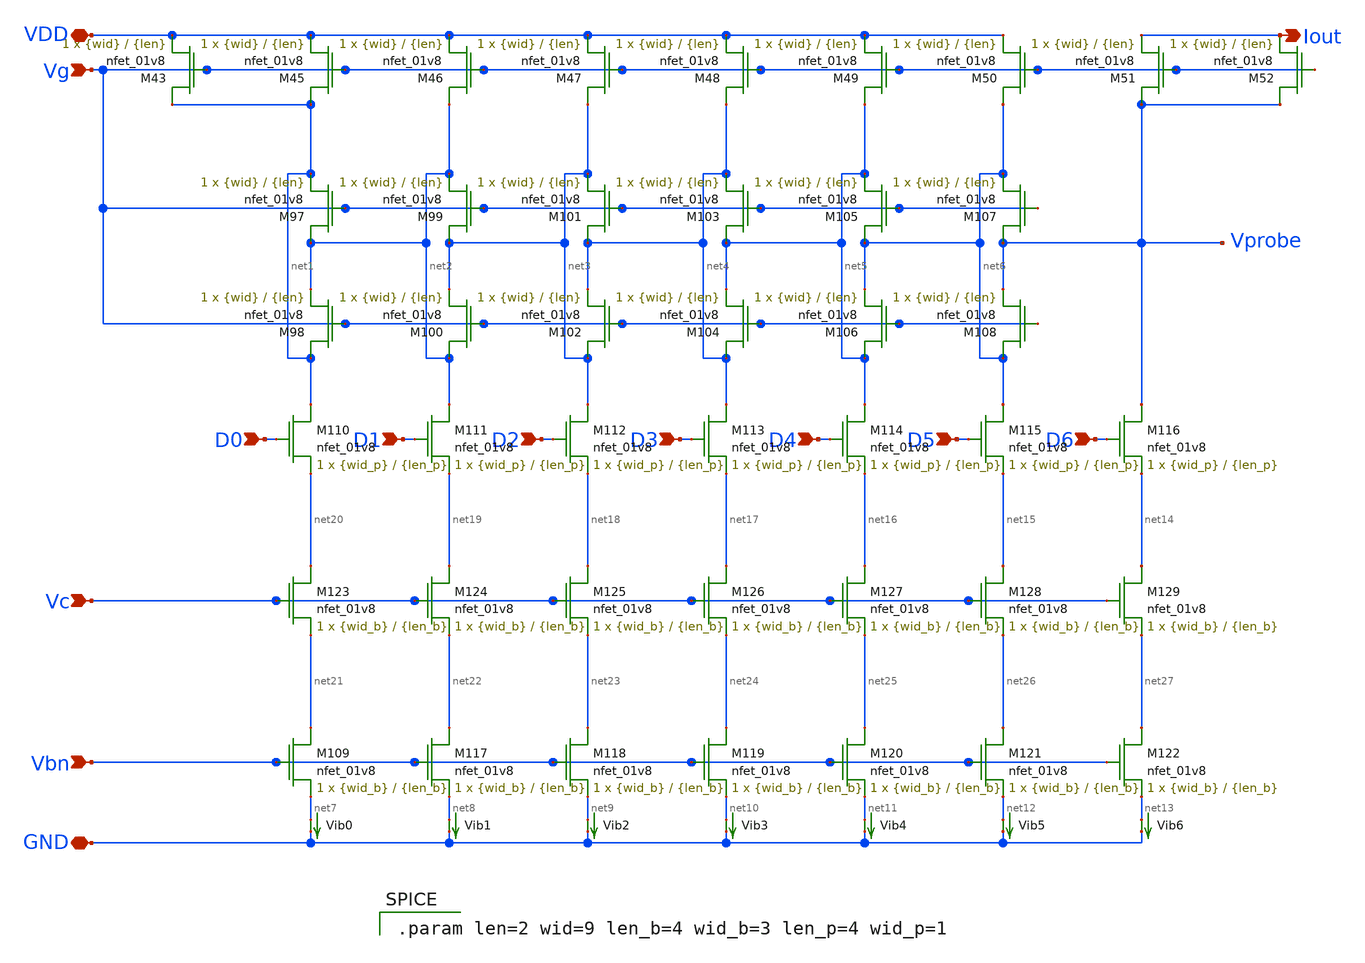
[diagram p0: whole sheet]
** sch_path: mp3/Layout_Schem_Designs/ladder_lds.sch
**.subckt ladder_lds VDD Iout Vg Vbn GND D0 D1 D2 D3 D4 D5 D6 Vc
*.iopin VDD
*.opin Iout
*.ipin Vg
*.ipin Vbn
*.iopin GND
*.ipin D0
*.ipin D1
*.ipin D2
*.ipin D3
*.ipin D4
*.ipin D5
*.ipin D6
*.ipin Vc
XM43 net1 Vg VDD GND sky130_fd_pr__nfet_01v8 L={len} W={wid} nf=1 ad='int((nf+1)/2) * W/nf * 0.29' as='int((nf+2)/2) * W/nf * 0.29'
+ pd='2*int((nf+1)/2) * (W/nf + 0.29)' ps='2*int((nf+2)/2) * (W/nf + 0.29)' nrd='0.29 / W' nrs='0.29 / W'
+ sa=0 sb=0 sd=0 mult=1 m=1
XM45 net1 Vg VDD GND sky130_fd_pr__nfet_01v8 L={len} W={wid} nf=1 ad='int((nf+1)/2) * W/nf * 0.29' as='int((nf+2)/2) * W/nf * 0.29'
+ pd='2*int((nf+1)/2) * (W/nf + 0.29)' ps='2*int((nf+2)/2) * (W/nf + 0.29)' nrd='0.29 / W' nrs='0.29 / W'
+ sa=0 sb=0 sd=0 mult=1 m=1
XM46 net2 Vg VDD GND sky130_fd_pr__nfet_01v8 L={len} W={wid} nf=1 ad='int((nf+1)/2) * W/nf * 0.29' as='int((nf+2)/2) * W/nf * 0.29'
+ pd='2*int((nf+1)/2) * (W/nf + 0.29)' ps='2*int((nf+2)/2) * (W/nf + 0.29)' nrd='0.29 / W' nrs='0.29 / W'
+ sa=0 sb=0 sd=0 mult=1 m=1
XM47 net3 Vg VDD GND sky130_fd_pr__nfet_01v8 L={len} W={wid} nf=1 ad='int((nf+1)/2) * W/nf * 0.29' as='int((nf+2)/2) * W/nf * 0.29'
+ pd='2*int((nf+1)/2) * (W/nf + 0.29)' ps='2*int((nf+2)/2) * (W/nf + 0.29)' nrd='0.29 / W' nrs='0.29 / W'
+ sa=0 sb=0 sd=0 mult=1 m=1
XM48 net4 Vg VDD GND sky130_fd_pr__nfet_01v8 L={len} W={wid} nf=1 ad='int((nf+1)/2) * W/nf * 0.29' as='int((nf+2)/2) * W/nf * 0.29'
+ pd='2*int((nf+1)/2) * (W/nf + 0.29)' ps='2*int((nf+2)/2) * (W/nf + 0.29)' nrd='0.29 / W' nrs='0.29 / W'
+ sa=0 sb=0 sd=0 mult=1 m=1
XM49 net5 Vg VDD GND sky130_fd_pr__nfet_01v8 L={len} W={wid} nf=1 ad='int((nf+1)/2) * W/nf * 0.29' as='int((nf+2)/2) * W/nf * 0.29'
+ pd='2*int((nf+1)/2) * (W/nf + 0.29)' ps='2*int((nf+2)/2) * (W/nf + 0.29)' nrd='0.29 / W' nrs='0.29 / W'
+ sa=0 sb=0 sd=0 mult=1 m=1
XM50 net6 Vg VDD GND sky130_fd_pr__nfet_01v8 L={len} W={wid} nf=1 ad='int((nf+1)/2) * W/nf * 0.29' as='int((nf+2)/2) * W/nf * 0.29'
+ pd='2*int((nf+1)/2) * (W/nf + 0.29)' ps='2*int((nf+2)/2) * (W/nf + 0.29)' nrd='0.29 / W' nrs='0.29 / W'
+ sa=0 sb=0 sd=0 mult=1 m=1
XM51 Vprobe Vg Iout GND sky130_fd_pr__nfet_01v8 L={len} W={wid} nf=1 ad='int((nf+1)/2) * W/nf * 0.29'
+ as='int((nf+2)/2) * W/nf * 0.29' pd='2*int((nf+1)/2) * (W/nf + 0.29)' ps='2*int((nf+2)/2) * (W/nf + 0.29)'
+ nrd='0.29 / W' nrs='0.29 / W' sa=0 sb=0 sd=0 mult=1 m=1
XM52 Vprobe Vg Iout GND sky130_fd_pr__nfet_01v8 L={len} W={wid} nf=1 ad='int((nf+1)/2) * W/nf * 0.29'
+ as='int((nf+2)/2) * W/nf * 0.29' pd='2*int((nf+1)/2) * (W/nf + 0.29)' ps='2*int((nf+2)/2) * (W/nf + 0.29)'
+ nrd='0.29 / W' nrs='0.29 / W' sa=0 sb=0 sd=0 mult=1 m=1
XM97 net2 Vg net1 GND sky130_fd_pr__nfet_01v8 L={len} W={wid} nf=1 ad='int((nf+1)/2) * W/nf * 0.29' as='int((nf+2)/2) * W/nf * 0.29'
+ pd='2*int((nf+1)/2) * (W/nf + 0.29)' ps='2*int((nf+2)/2) * (W/nf + 0.29)' nrd='0.29 / W' nrs='0.29 / W'
+ sa=0 sb=0 sd=0 mult=1 m=1
XM98 net1 Vg net2 GND sky130_fd_pr__nfet_01v8 L={len} W={wid} nf=1 ad='int((nf+1)/2) * W/nf * 0.29' as='int((nf+2)/2) * W/nf * 0.29'
+ pd='2*int((nf+1)/2) * (W/nf + 0.29)' ps='2*int((nf+2)/2) * (W/nf + 0.29)' nrd='0.29 / W' nrs='0.29 / W'
+ sa=0 sb=0 sd=0 mult=1 m=1
XM99 net3 Vg net2 GND sky130_fd_pr__nfet_01v8 L={len} W={wid} nf=1 ad='int((nf+1)/2) * W/nf * 0.29' as='int((nf+2)/2) * W/nf * 0.29'
+ pd='2*int((nf+1)/2) * (W/nf + 0.29)' ps='2*int((nf+2)/2) * (W/nf + 0.29)' nrd='0.29 / W' nrs='0.29 / W'
+ sa=0 sb=0 sd=0 mult=1 m=1
XM100 net2 Vg net3 GND sky130_fd_pr__nfet_01v8 L={len} W={wid} nf=1 ad='int((nf+1)/2) * W/nf * 0.29'
+ as='int((nf+2)/2) * W/nf * 0.29' pd='2*int((nf+1)/2) * (W/nf + 0.29)' ps='2*int((nf+2)/2) * (W/nf + 0.29)'
+ nrd='0.29 / W' nrs='0.29 / W' sa=0 sb=0 sd=0 mult=1 m=1
XM101 net4 Vg net3 GND sky130_fd_pr__nfet_01v8 L={len} W={wid} nf=1 ad='int((nf+1)/2) * W/nf * 0.29'
+ as='int((nf+2)/2) * W/nf * 0.29' pd='2*int((nf+1)/2) * (W/nf + 0.29)' ps='2*int((nf+2)/2) * (W/nf + 0.29)'
+ nrd='0.29 / W' nrs='0.29 / W' sa=0 sb=0 sd=0 mult=1 m=1
XM102 net3 Vg net4 GND sky130_fd_pr__nfet_01v8 L={len} W={wid} nf=1 ad='int((nf+1)/2) * W/nf * 0.29'
+ as='int((nf+2)/2) * W/nf * 0.29' pd='2*int((nf+1)/2) * (W/nf + 0.29)' ps='2*int((nf+2)/2) * (W/nf + 0.29)'
+ nrd='0.29 / W' nrs='0.29 / W' sa=0 sb=0 sd=0 mult=1 m=1
XM103 net5 Vg net4 GND sky130_fd_pr__nfet_01v8 L={len} W={wid} nf=1 ad='int((nf+1)/2) * W/nf * 0.29'
+ as='int((nf+2)/2) * W/nf * 0.29' pd='2*int((nf+1)/2) * (W/nf + 0.29)' ps='2*int((nf+2)/2) * (W/nf + 0.29)'
+ nrd='0.29 / W' nrs='0.29 / W' sa=0 sb=0 sd=0 mult=1 m=1
XM104 net4 Vg net5 GND sky130_fd_pr__nfet_01v8 L={len} W={wid} nf=1 ad='int((nf+1)/2) * W/nf * 0.29'
+ as='int((nf+2)/2) * W/nf * 0.29' pd='2*int((nf+1)/2) * (W/nf + 0.29)' ps='2*int((nf+2)/2) * (W/nf + 0.29)'
+ nrd='0.29 / W' nrs='0.29 / W' sa=0 sb=0 sd=0 mult=1 m=1
XM105 net6 Vg net5 GND sky130_fd_pr__nfet_01v8 L={len} W={wid} nf=1 ad='int((nf+1)/2) * W/nf * 0.29'
+ as='int((nf+2)/2) * W/nf * 0.29' pd='2*int((nf+1)/2) * (W/nf + 0.29)' ps='2*int((nf+2)/2) * (W/nf + 0.29)'
+ nrd='0.29 / W' nrs='0.29 / W' sa=0 sb=0 sd=0 mult=1 m=1
XM106 net5 Vg net6 GND sky130_fd_pr__nfet_01v8 L={len} W={wid} nf=1 ad='int((nf+1)/2) * W/nf * 0.29'
+ as='int((nf+2)/2) * W/nf * 0.29' pd='2*int((nf+1)/2) * (W/nf + 0.29)' ps='2*int((nf+2)/2) * (W/nf + 0.29)'
+ nrd='0.29 / W' nrs='0.29 / W' sa=0 sb=0 sd=0 mult=1 m=1
XM107 Vprobe Vg net6 GND sky130_fd_pr__nfet_01v8 L={len} W={wid} nf=1 ad='int((nf+1)/2) * W/nf * 0.29'
+ as='int((nf+2)/2) * W/nf * 0.29' pd='2*int((nf+1)/2) * (W/nf + 0.29)' ps='2*int((nf+2)/2) * (W/nf + 0.29)'
+ nrd='0.29 / W' nrs='0.29 / W' sa=0 sb=0 sd=0 mult=1 m=1
XM108 net6 Vg Vprobe GND sky130_fd_pr__nfet_01v8 L={len} W={wid} nf=1 ad='int((nf+1)/2) * W/nf * 0.29'
+ as='int((nf+2)/2) * W/nf * 0.29' pd='2*int((nf+1)/2) * (W/nf + 0.29)' ps='2*int((nf+2)/2) * (W/nf + 0.29)'
+ nrd='0.29 / W' nrs='0.29 / W' sa=0 sb=0 sd=0 mult=1 m=1
XM109 net21 Vbn net7 GND sky130_fd_pr__nfet_01v8 L={len_b} W={wid_b} nf=1 ad='int((nf+1)/2) * W/nf * 0.29'
+ as='int((nf+2)/2) * W/nf * 0.29' pd='2*int((nf+1)/2) * (W/nf + 0.29)' ps='2*int((nf+2)/2) * (W/nf + 0.29)'
+ nrd='0.29 / W' nrs='0.29 / W' sa=0 sb=0 sd=0 mult=1 m=1
Vib0 net7 GND 0
.save i(vib0)
XM110 net1 D0 net20 GND sky130_fd_pr__nfet_01v8 L={len_p} W={wid_p} nf=1 ad='int((nf+1)/2) * W/nf * 0.29'
+ as='int((nf+2)/2) * W/nf * 0.29' pd='2*int((nf+1)/2) * (W/nf + 0.29)' ps='2*int((nf+2)/2) * (W/nf + 0.29)'
+ nrd='0.29 / W' nrs='0.29 / W' sa=0 sb=0 sd=0 mult=1 m=1
XM111 net2 D1 net19 GND sky130_fd_pr__nfet_01v8 L={len_p} W={wid_p} nf=1 ad='int((nf+1)/2) * W/nf * 0.29'
+ as='int((nf+2)/2) * W/nf * 0.29' pd='2*int((nf+1)/2) * (W/nf + 0.29)' ps='2*int((nf+2)/2) * (W/nf + 0.29)'
+ nrd='0.29 / W' nrs='0.29 / W' sa=0 sb=0 sd=0 mult=1 m=1
XM112 net3 D2 net18 GND sky130_fd_pr__nfet_01v8 L={len_p} W={wid_p} nf=1 ad='int((nf+1)/2) * W/nf * 0.29'
+ as='int((nf+2)/2) * W/nf * 0.29' pd='2*int((nf+1)/2) * (W/nf + 0.29)' ps='2*int((nf+2)/2) * (W/nf + 0.29)'
+ nrd='0.29 / W' nrs='0.29 / W' sa=0 sb=0 sd=0 mult=1 m=1
XM113 net4 D3 net17 GND sky130_fd_pr__nfet_01v8 L={len_p} W={wid_p} nf=1 ad='int((nf+1)/2) * W/nf * 0.29'
+ as='int((nf+2)/2) * W/nf * 0.29' pd='2*int((nf+1)/2) * (W/nf + 0.29)' ps='2*int((nf+2)/2) * (W/nf + 0.29)'
+ nrd='0.29 / W' nrs='0.29 / W' sa=0 sb=0 sd=0 mult=1 m=1
XM114 net5 D4 net16 GND sky130_fd_pr__nfet_01v8 L={len_p} W={wid_p} nf=1 ad='int((nf+1)/2) * W/nf * 0.29'
+ as='int((nf+2)/2) * W/nf * 0.29' pd='2*int((nf+1)/2) * (W/nf + 0.29)' ps='2*int((nf+2)/2) * (W/nf + 0.29)'
+ nrd='0.29 / W' nrs='0.29 / W' sa=0 sb=0 sd=0 mult=1 m=1
XM115 net6 D5 net15 GND sky130_fd_pr__nfet_01v8 L={len_p} W={wid_p} nf=1 ad='int((nf+1)/2) * W/nf * 0.29'
+ as='int((nf+2)/2) * W/nf * 0.29' pd='2*int((nf+1)/2) * (W/nf + 0.29)' ps='2*int((nf+2)/2) * (W/nf + 0.29)'
+ nrd='0.29 / W' nrs='0.29 / W' sa=0 sb=0 sd=0 mult=1 m=1
XM116 Vprobe D6 net14 GND sky130_fd_pr__nfet_01v8 L={len_p} W={wid_p} nf=1 ad='int((nf+1)/2) * W/nf * 0.29'
+ as='int((nf+2)/2) * W/nf * 0.29' pd='2*int((nf+1)/2) * (W/nf + 0.29)' ps='2*int((nf+2)/2) * (W/nf + 0.29)'
+ nrd='0.29 / W' nrs='0.29 / W' sa=0 sb=0 sd=0 mult=1 m=1
XM117 net22 Vbn net8 GND sky130_fd_pr__nfet_01v8 L={len_b} W={wid_b} nf=1 ad='int((nf+1)/2) * W/nf * 0.29'
+ as='int((nf+2)/2) * W/nf * 0.29' pd='2*int((nf+1)/2) * (W/nf + 0.29)' ps='2*int((nf+2)/2) * (W/nf + 0.29)'
+ nrd='0.29 / W' nrs='0.29 / W' sa=0 sb=0 sd=0 mult=1 m=1
XM118 net23 Vbn net9 GND sky130_fd_pr__nfet_01v8 L={len_b} W={wid_b} nf=1 ad='int((nf+1)/2) * W/nf * 0.29'
+ as='int((nf+2)/2) * W/nf * 0.29' pd='2*int((nf+1)/2) * (W/nf + 0.29)' ps='2*int((nf+2)/2) * (W/nf + 0.29)'
+ nrd='0.29 / W' nrs='0.29 / W' sa=0 sb=0 sd=0 mult=1 m=1
XM119 net24 Vbn net10 GND sky130_fd_pr__nfet_01v8 L={len_b} W={wid_b} nf=1 ad='int((nf+1)/2) * W/nf * 0.29'
+ as='int((nf+2)/2) * W/nf * 0.29' pd='2*int((nf+1)/2) * (W/nf + 0.29)' ps='2*int((nf+2)/2) * (W/nf + 0.29)'
+ nrd='0.29 / W' nrs='0.29 / W' sa=0 sb=0 sd=0 mult=1 m=1
XM120 net25 Vbn net11 GND sky130_fd_pr__nfet_01v8 L={len_b} W={wid_b} nf=1 ad='int((nf+1)/2) * W/nf * 0.29'
+ as='int((nf+2)/2) * W/nf * 0.29' pd='2*int((nf+1)/2) * (W/nf + 0.29)' ps='2*int((nf+2)/2) * (W/nf + 0.29)'
+ nrd='0.29 / W' nrs='0.29 / W' sa=0 sb=0 sd=0 mult=1 m=1
XM121 net26 Vbn net12 GND sky130_fd_pr__nfet_01v8 L={len_b} W={wid_b} nf=1 ad='int((nf+1)/2) * W/nf * 0.29'
+ as='int((nf+2)/2) * W/nf * 0.29' pd='2*int((nf+1)/2) * (W/nf + 0.29)' ps='2*int((nf+2)/2) * (W/nf + 0.29)'
+ nrd='0.29 / W' nrs='0.29 / W' sa=0 sb=0 sd=0 mult=1 m=1
XM122 net27 Vbn net13 GND sky130_fd_pr__nfet_01v8 L={len_b} W={wid_b} nf=1 ad='int((nf+1)/2) * W/nf * 0.29'
+ as='int((nf+2)/2) * W/nf * 0.29' pd='2*int((nf+1)/2) * (W/nf + 0.29)' ps='2*int((nf+2)/2) * (W/nf + 0.29)'
+ nrd='0.29 / W' nrs='0.29 / W' sa=0 sb=0 sd=0 mult=1 m=1
XM123 net20 Vc net21 GND sky130_fd_pr__nfet_01v8 L={len_b} W={wid_b} nf=1 ad='int((nf+1)/2) * W/nf * 0.29'
+ as='int((nf+2)/2) * W/nf * 0.29' pd='2*int((nf+1)/2) * (W/nf + 0.29)' ps='2*int((nf+2)/2) * (W/nf + 0.29)'
+ nrd='0.29 / W' nrs='0.29 / W' sa=0 sb=0 sd=0 mult=1 m=1
XM124 net19 Vc net22 GND sky130_fd_pr__nfet_01v8 L={len_b} W={wid_b} nf=1 ad='int((nf+1)/2) * W/nf * 0.29'
+ as='int((nf+2)/2) * W/nf * 0.29' pd='2*int((nf+1)/2) * (W/nf + 0.29)' ps='2*int((nf+2)/2) * (W/nf + 0.29)'
+ nrd='0.29 / W' nrs='0.29 / W' sa=0 sb=0 sd=0 mult=1 m=1
XM125 net18 Vc net23 GND sky130_fd_pr__nfet_01v8 L={len_b} W={wid_b} nf=1 ad='int((nf+1)/2) * W/nf * 0.29'
+ as='int((nf+2)/2) * W/nf * 0.29' pd='2*int((nf+1)/2) * (W/nf + 0.29)' ps='2*int((nf+2)/2) * (W/nf + 0.29)'
+ nrd='0.29 / W' nrs='0.29 / W' sa=0 sb=0 sd=0 mult=1 m=1
XM126 net17 Vc net24 GND sky130_fd_pr__nfet_01v8 L={len_b} W={wid_b} nf=1 ad='int((nf+1)/2) * W/nf * 0.29'
+ as='int((nf+2)/2) * W/nf * 0.29' pd='2*int((nf+1)/2) * (W/nf + 0.29)' ps='2*int((nf+2)/2) * (W/nf + 0.29)'
+ nrd='0.29 / W' nrs='0.29 / W' sa=0 sb=0 sd=0 mult=1 m=1
XM127 net16 Vc net25 GND sky130_fd_pr__nfet_01v8 L={len_b} W={wid_b} nf=1 ad='int((nf+1)/2) * W/nf * 0.29'
+ as='int((nf+2)/2) * W/nf * 0.29' pd='2*int((nf+1)/2) * (W/nf + 0.29)' ps='2*int((nf+2)/2) * (W/nf + 0.29)'
+ nrd='0.29 / W' nrs='0.29 / W' sa=0 sb=0 sd=0 mult=1 m=1
XM128 net15 Vc net26 GND sky130_fd_pr__nfet_01v8 L={len_b} W={wid_b} nf=1 ad='int((nf+1)/2) * W/nf * 0.29'
+ as='int((nf+2)/2) * W/nf * 0.29' pd='2*int((nf+1)/2) * (W/nf + 0.29)' ps='2*int((nf+2)/2) * (W/nf + 0.29)'
+ nrd='0.29 / W' nrs='0.29 / W' sa=0 sb=0 sd=0 mult=1 m=1
XM129 net14 Vc net27 GND sky130_fd_pr__nfet_01v8 L={len_b} W={wid_b} nf=1 ad='int((nf+1)/2) * W/nf * 0.29'
+ as='int((nf+2)/2) * W/nf * 0.29' pd='2*int((nf+1)/2) * (W/nf + 0.29)' ps='2*int((nf+2)/2) * (W/nf + 0.29)'
+ nrd='0.29 / W' nrs='0.29 / W' sa=0 sb=0 sd=0 mult=1 m=1
Vib1 net8 GND 0
.save i(vib1)
Vib2 net9 GND 0
.save i(vib2)
Vib3 net10 GND 0
.save i(vib3)
Vib4 net11 GND 0
.save i(vib4)
Vib5 net12 GND 0
.save i(vib5)
Vib6 net13 GND 0
.save i(vib6)
**** begin user architecture code

.param len=2 wid=9 len_b=4 wid_b=3 len_p=4 wid_p=1

**** end user architecture code
**.ends
.end
